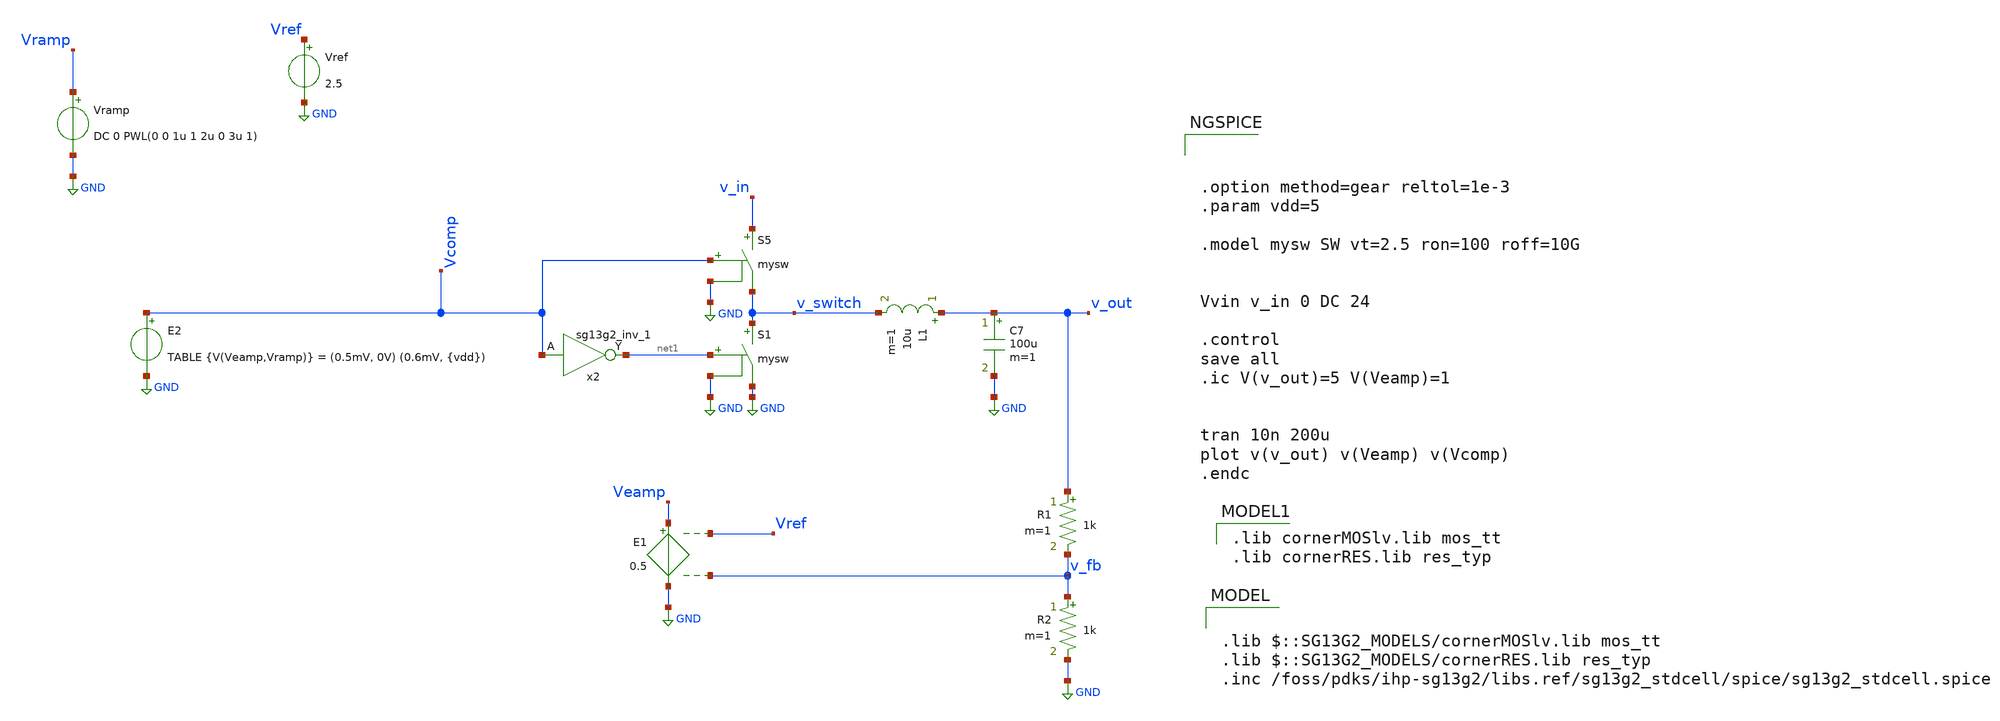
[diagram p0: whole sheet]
** sch_path: Designs/ideal_circuits/ideal_dcdc.sch
* (c) 2025 Thesis_HP, Apache-2.0 license
**.subckt ideal_dcdc
Vramp Vramp GND DC 0 PWL(0 0 1u 1 2u 0 3u 1)
S5 v_in v_switch Vcomp GND mysw
S1 v_switch GND net1 GND mysw
L1 v_out v_switch 10u m=1
C7 v_out GND 100u m=1
R1 v_out v_fb 1k m=1
R2 v_fb GND 1k m=1
Vref Vref GND 2.5
x2 net1 Vcomp 1.5 0 sg13g2_inv_1
E1 Veamp GND Vref v_fb 0.5
E2 Vcomp GND TABLE {V(Veamp,Vramp)} = (0.5mV, 0V) (0.6mV, {vdd})
**** begin user architecture code



.option method=gear reltol=1e-3
.param vdd=5

.model mysw SW vt=2.5 ron=100 roff=10G


Vvin v_in 0 DC 24

.control
save all
.ic V(v_out)=5 V(Veamp)=1


tran 10n 200u
plot v(v_out) v(Veamp) v(Vcomp)
.endc


 .lib cornerMOSlv.lib mos_tt
.lib cornerRES.lib res_typ


.lib $::SG13G2_MODELS/cornerMOSlv.lib mos_tt
.lib $::SG13G2_MODELS/cornerRES.lib res_typ
.inc /foss/pdks/ihp-sg13g2/libs.ref/sg13g2_stdcell/spice/sg13g2_stdcell.spice

**** end user architecture code
**.ends

* expanding   symbol:  sg13g2_stdcells/sg13g2_inv_1.sym # of pins=2
** sym_path: sg13g2_stdcells/sg13g2_inv_1.sym
** sch_path: sg13g2_stdcells/sg13g2_inv_1.sch
.subckt sg13g2_inv_1 Y A VDD VSS
*.opin Y
*.ipin A
*.iopin VDD
*.iopin VSS
XM1 Y A VSS VSS sg13_lv_nmos w=740.00n l=130.00n ng=1 m=1 mm_ok=1
XM2 Y A VDD VDD sg13_lv_pmos w=1.12u l=130.00n ng=1 m=1 mm_ok=1
.ends

.GLOBAL GND
.end
